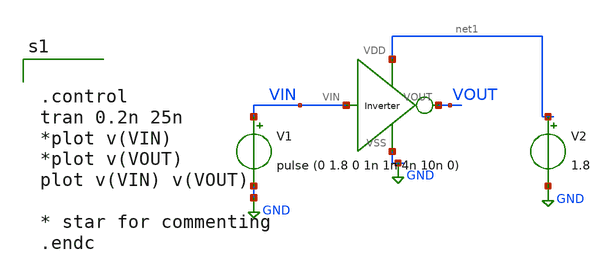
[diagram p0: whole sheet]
** sch_path: xschem/xschem_BGR_Top/Sigma_Delta/Inverter/Inverter_TB.sch
**.subckt Inverter_TB
V1 VIN GND pulse (0 1.8 0 1n 1n 4n 10n 0)
V2 net1 GND 1.8
X1 GND net1 VIN VOUT Inverter
**** begin user architecture code


.control
tran 0.2n 25n
*plot v(VIN)
*plot v(VOUT)
plot v(VIN) v(VOUT)

* star for commenting
.endc


** opencircuitdesign pdks install
.lib $::SKYWATER_MODELS/sky130.lib.spice tt


**** end user architecture code
**.ends

* expanding   symbol:  Sigma_Delta/Inverter/Inverter.sym # of pins=4
** sym_path: xschem/xschem_BGR_Top/Sigma_Delta/Inverter/Inverter.sym
** sch_path: xschem/xschem_BGR_Top/Sigma_Delta/Inverter/Inverter.sch
.subckt Inverter VSS VDD VIN VOUT
*.ipin VIN
*.iopin VDD
*.iopin VSS
*.opin VOUT
XM1 VOUT VIN VSS VSS sky130_fd_pr__nfet_01v8 L=0.15 W=0.9 nf=1 ad='int((nf+1)/2) * W/nf * 0.29' as='int((nf+2)/2) * W/nf * 0.29'
+ pd='2*int((nf+1)/2) * (W/nf + 0.29)' ps='2*int((nf+2)/2) * (W/nf + 0.29)' nrd='0.29 / W' nrs='0.29 / W'
+ sa=0 sb=0 sd=0 mult=1 m=1
XM2 VOUT VIN VDD VDD sky130_fd_pr__pfet_01v8 L=0.15 W=0.9 nf=2 ad='int((nf+1)/2) * W/nf * 0.29' as='int((nf+2)/2) * W/nf * 0.29'
+ pd='2*int((nf+1)/2) * (W/nf + 0.29)' ps='2*int((nf+2)/2) * (W/nf + 0.29)' nrd='0.29 / W' nrs='0.29 / W'
+ sa=0 sb=0 sd=0 mult=1 m=1
.ends

.GLOBAL GND
.end
